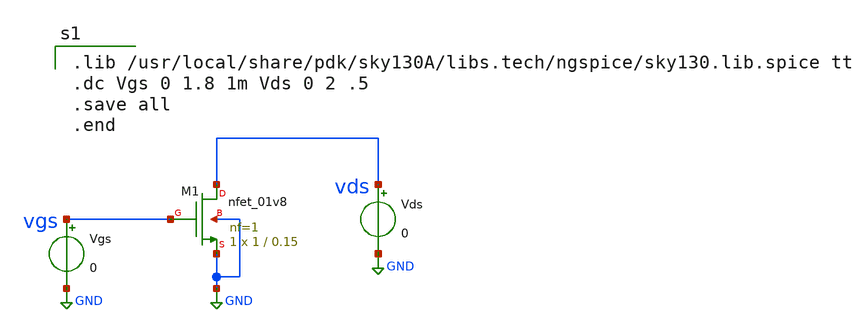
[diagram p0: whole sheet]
** sch_path: VLSI/VLSI_TEST_02/dc_sweep.sch
**.subckt dc_sweep
XM1 vds vgs GND GND sky130_fd_pr__nfet_01v8 L=0.15 W=1 nf=1 ad='int((nf+1)/2) * W/nf * 0.29' as='int((nf+2)/2) * W/nf * 0.29'
+ pd='2*int((nf+1)/2) * (W/nf + 0.29)' ps='2*int((nf+2)/2) * (W/nf + 0.29)' nrd='0.29 / W' nrs='0.29 / W'
+ sa=0 sb=0 sd=0 mult=1 m=1
Vgs vgs GND 0
Vds vds GND 0
**** begin user architecture code

.lib /usr/local/share/pdk/sky130A/libs.tech/ngspice/sky130.lib.spice tt
.dc Vgs 0 1.8 1m Vds 0 2 .5
.save all
.end

**** end user architecture code
**.ends
.GLOBAL GND
.end
